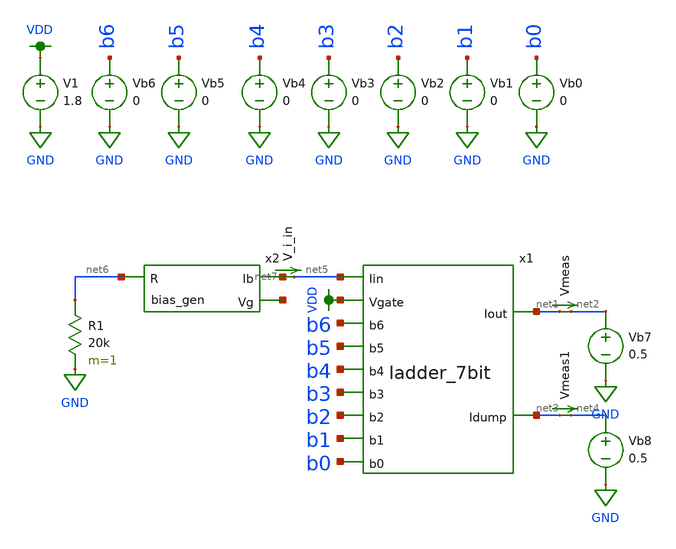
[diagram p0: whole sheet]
** sch_path: test_harness_mc.sch
**.subckt test_harness_mc
x1 VDD net5 net3 net1 b5 b4 b1 b2 b3 b0 b6 ladder_7bit
Vmeas net1 net2 0
.save i(vmeas)
Vb0 b0 GND 0
Vb1 b1 GND 0
Vb2 b2 GND 0
Vb3 b3 GND 0
Vb4 b4 GND 0
Vb5 b5 GND 0
Vb6 b6 GND 0
V1 VDD GND 1.8
Vb7 net2 GND 0.5
Vb8 net4 GND 0.5
Vmeas1 net3 net4 0
.save i(vmeas1)
V_i_in net7 net5 0
.save i(v_i_in)
x2 net7 net8 net6 bias_gen
R1 net6 GND 20k m=1
**** begin user architecture code

.option wnflag=1
.param MC_SWITCH=0.0
.lib ~/skywater/skywater-pdk/libraries/sky130_fd_pr_ngspice/latest/models/sky130.lib.spice tt


.control
  let runs = 10
  let run = 1
  while run <= runs
    set appendwrite = FALSE
    set wr_vecnames
    let code = 0
    while code < 128
      if code eq 0
        let b0 = 0
      else
        let b0 = code % 2
      end
      if floor(code / 2) eq 0
        let b1 = 0
      else
        let b1 = floor(code / 2) % 2
      end
      if floor(code / 4) eq 0
        let b2 = 0
      else
        let b2 = floor(code / 4) % 2
      end
      if floor(code / 8) eq 0
        let b3 = 0
      else
        let b3 = floor(code / 8) % 2
      end
      if floor(code / 16) eq 0
        let b4 = 0
      else
        let b4 = floor(code / 16) % 2
      end
      if floor(code / 32) eq 0
        let b5 = 0
      else
        let b5 = floor(code / 32) % 2
      end
      if floor(code / 64) eq 0
        let b6 = 0
      else
        let b6 = floor(code / 64) % 2
      end
      alter vb0 1.8*$&b0
      alter vb1 1.8*$&b1
      alter vb2 1.8*$&b2
      alter vb3 1.8*$&b3
      alter vb4 1.8*$&b4
      alter vb5 1.8*$&b5
      alter vb6 1.8*$&b6
      save all
      op
      wrdata ~/Documents/dac/mcdac{$&run}.txt v(b0) v(b1) v(b2) v(b3) v(b4) v(b5) v(b6) i(V_i_in) i(Vmeas)
+ i(Vmeas1)
      if code eq 0
        set appendwrite
        set wr_vecnames = FALSE
      end
      let code = code + 1
    end
    reset
    let run = run + 1
  end
.endc

**** end user architecture code
**.ends

* expanding   symbol:  ./ladder_7bit.sym # of pins=11
** sym_path: ladder_7bit.sym
** sch_path: ladder_7bit.sch
.subckt ladder_7bit Vgate Iin Idump Iout b5 b4 b1 b2 b3 b0 b6
*.opin Idump
*.opin Iout
*.ipin Vgate
*.ipin Iin
*.ipin b6
*.ipin b5
*.ipin b4
*.ipin b3
*.ipin b2
*.ipin b1
*.ipin b0
x1 Iin net8 Vgate Idump Iout net1 b6 ladder_1bit
x2 net8 net9 Vgate Idump Iout net2 b5 ladder_1bit
x3 net9 net10 Vgate Idump Iout net3 b4 ladder_1bit
x4 net10 net11 Vgate Idump Iout net4 b3 ladder_1bit
x5 net11 net12 Vgate Idump Iout net5 b2 ladder_1bit
x6 net12 net13 Vgate Idump Iout net6 b1 ladder_1bit
x7 net13 net14 Vgate Idump Iout net7 b0 ladder_1bit
XM1 Idump Vgate net14 GND sky130_fd_pr__nfet_01v8 L=0.15 W=1 nf=1 ad='int((nf+1)/2) * W/nf * 0.29' as='int((nf+2)/2) * W/nf * 0.29'
+ pd='2*int((nf+1)/2) * (W/nf + 0.29)' ps='2*int((nf+2)/2) * (W/nf + 0.29)' nrd='0.29 / W' nrs='0.29 / W'
+ sa=0 sb=0 sd=0 mult=1 m=1
X8 b6 net15 VDD GND inverter
X9 b5 net16 VDD GND inverter
X10 b4 net17 VDD GND inverter
X11 b3 net18 VDD GND inverter
X12 b2 net19 VDD GND inverter
X13 b1 net20 VDD GND inverter
X14 b0 net21 VDD GND inverter
.ends


* expanding   symbol:  ./bias_gen.sym # of pins=3
** sym_path: bias_gen.sym
** sch_path: bias_gen.sch
.subckt bias_gen Ib Vg R
*.ipin R
*.opin Ib
*.opin Vg
XM2 R net2 net2 GND sky130_fd_pr__nfet_01v8 L=4 W=96 nf=1 ad='int((nf+1)/2) * W/nf * 0.29' as='int((nf+2)/2) * W/nf * 0.29'
+ pd='2*int((nf+1)/2) * (W/nf + 0.29)' ps='2*int((nf+2)/2) * (W/nf + 0.29)' nrd='0.29 / W' nrs='0.29 / W'
+ sa=0 sb=0 sd=0 mult=1 m=1
XM3 VDD net1 net1 VDD sky130_fd_pr__pfet_01v8 L=4 W=12 nf=1 ad='int((nf+1)/2) * W/nf * 0.29' as='int((nf+2)/2) * W/nf * 0.29'
+ pd='2*int((nf+1)/2) * (W/nf + 0.29)' ps='2*int((nf+2)/2) * (W/nf + 0.29)' nrd='0.29 / W' nrs='0.29 / W'
+ sa=0 sb=0 sd=0 mult=1 m=1
XM1 VDD Vg net2 VDD sky130_fd_pr__pfet_01v8 L=4 W=12 nf=1 ad='int((nf+1)/2) * W/nf * 0.29' as='int((nf+2)/2) * W/nf * 0.29'
+ pd='2*int((nf+1)/2) * (W/nf + 0.29)' ps='2*int((nf+2)/2) * (W/nf + 0.29)' nrd='0.29 / W' nrs='0.29 / W'
+ sa=0 sb=0 sd=0 mult=1 m=1
XM4 Vg net1 VDD VDD sky130_fd_pr__pfet_01v8 L=4 W=12 nf=1 ad='int((nf+1)/2) * W/nf * 0.29' as='int((nf+2)/2) * W/nf * 0.29'
+ pd='2*int((nf+1)/2) * (W/nf + 0.29)' ps='2*int((nf+2)/2) * (W/nf + 0.29)' nrd='0.29 / W' nrs='0.29 / W'
+ sa=0 sb=0 sd=0 mult=1 m=1
XM5 net3 Vg VDD VDD sky130_fd_pr__pfet_01v8 L=4 W=12 nf=1 ad='int((nf+1)/2) * W/nf * 0.29' as='int((nf+2)/2) * W/nf * 0.29'
+ pd='2*int((nf+1)/2) * (W/nf + 0.29)' ps='2*int((nf+2)/2) * (W/nf + 0.29)' nrd='0.29 / W' nrs='0.29 / W'
+ sa=0 sb=0 sd=0 mult=1 m=1
XM7 Ib Vg VDD VDD sky130_fd_pr__pfet_01v8 L=4 W=12 nf=1 ad='int((nf+1)/2) * W/nf * 0.29' as='int((nf+2)/2) * W/nf * 0.29'
+ pd='2*int((nf+1)/2) * (W/nf + 0.29)' ps='2*int((nf+2)/2) * (W/nf + 0.29)' nrd='0.29 / W' nrs='0.29 / W'
+ sa=0 sb=0 sd=0 mult=1 m=1
XM6 net1 net2 GND GND sky130_fd_pr__nfet_01v8 L=4 W=12 nf=1 ad='int((nf+1)/2) * W/nf * 0.29' as='int((nf+2)/2) * W/nf * 0.29'
+ pd='2*int((nf+1)/2) * (W/nf + 0.29)' ps='2*int((nf+2)/2) * (W/nf + 0.29)' nrd='0.29 / W' nrs='0.29 / W'
+ sa=0 sb=0 sd=0 mult=1 m=1
XM8 GND net3 Vg GND sky130_fd_pr__nfet_01v8 L=4 W=12 nf=1 ad='int((nf+1)/2) * W/nf * 0.29' as='int((nf+2)/2) * W/nf * 0.29'
+ pd='2*int((nf+1)/2) * (W/nf + 0.29)' ps='2*int((nf+2)/2) * (W/nf + 0.29)' nrd='0.29 / W' nrs='0.29 / W'
+ sa=0 sb=0 sd=0 mult=1 m=1
XM9 net3 net3 GND GND sky130_fd_pr__nfet_01v8 L=4 W=12 nf=1 ad='int((nf+1)/2) * W/nf * 0.29' as='int((nf+2)/2) * W/nf * 0.29'
+ pd='2*int((nf+1)/2) * (W/nf + 0.29)' ps='2*int((nf+2)/2) * (W/nf + 0.29)' nrd='0.29 / W' nrs='0.29 / W'
+ sa=0 sb=0 sd=0 mult=1 m=1
.ends


* expanding   symbol:  /home/madvlsi/R2R-DAC/ladder_1bit.sym # of pins=7
** sym_path: ladder_1bit.sym
** sch_path: ladder_1bit.sch
.subckt ladder_1bit Iin_in Iin_out Vg I_dump Iout B_bar B
*.ipin Iin_in
*.ipin Vg
*.ipin B
*.ipin B_bar
*.opin Iin_out
*.opin I_dump
*.opin Iout
XM5 net1 Vg Iin_in GND sky130_fd_pr__nfet_01v8 L=0.15 W=1 nf=1 ad='int((nf+1)/2) * W/nf * 0.29' as='int((nf+2)/2) * W/nf * 0.29'
+ pd='2*int((nf+1)/2) * (W/nf + 0.29)' ps='2*int((nf+2)/2) * (W/nf + 0.29)' nrd='0.29 / W' nrs='0.29 / W'
+ sa=0 sb=0 sd=0 mult=1 m=1
XM6 Iout B net1 GND sky130_fd_pr__nfet_01v8 L=0.15 W=1 nf=1 ad='int((nf+1)/2) * W/nf * 0.29' as='int((nf+2)/2) * W/nf * 0.29'
+ pd='2*int((nf+1)/2) * (W/nf + 0.29)' ps='2*int((nf+2)/2) * (W/nf + 0.29)' nrd='0.29 / W' nrs='0.29 / W'
+ sa=0 sb=0 sd=0 mult=1 m=1
XM7 net1 B_bar I_dump GND sky130_fd_pr__nfet_01v8 L=0.15 W=1 nf=1 ad='int((nf+1)/2) * W/nf * 0.29' as='int((nf+2)/2) * W/nf * 0.29'
+ pd='2*int((nf+1)/2) * (W/nf + 0.29)' ps='2*int((nf+2)/2) * (W/nf + 0.29)' nrd='0.29 / W' nrs='0.29 / W'
+ sa=0 sb=0 sd=0 mult=1 m=1
XM8 Iin_in Vg Iin_out GND sky130_fd_pr__nfet_01v8 L=0.15 W=1 nf=1 ad='int((nf+1)/2) * W/nf * 0.29' as='int((nf+2)/2) * W/nf * 0.29'
+ pd='2*int((nf+1)/2) * (W/nf + 0.29)' ps='2*int((nf+2)/2) * (W/nf + 0.29)' nrd='0.29 / W' nrs='0.29 / W'
+ sa=0 sb=0 sd=0 mult=1 m=1
.ends


* expanding   symbol:  /home/madvlsi/Documents/mp1/inverter.sym # of pins=4
** sym_path: /home/madvlsi/Documents/mp1/inverter.sym
** sch_path: /home/madvlsi/Documents/mp1/inverter.sch
.subckt inverter A Y VP VN
*.ipin A
*.iopin VP
*.iopin VN
*.opin Y
XM3 Y A VP VP sky130_fd_pr__pfet_01v8 L=0.15 W=1 nf=1 ad='int((nf+1)/2) * W/nf * 0.29' as='int((nf+2)/2) * W/nf * 0.29'
+ pd='2*int((nf+1)/2) * (W/nf + 0.29)' ps='2*int((nf+2)/2) * (W/nf + 0.29)' nrd='0.29 / W' nrs='0.29 / W'
+ sa=0 sb=0 sd=0 mult=1 m=1
XM4 Y A VN VN sky130_fd_pr__nfet_01v8 L=0.15 W=1 nf=1 ad='int((nf+1)/2) * W/nf * 0.29' as='int((nf+2)/2) * W/nf * 0.29'
+ pd='2*int((nf+1)/2) * (W/nf + 0.29)' ps='2*int((nf+2)/2) * (W/nf + 0.29)' nrd='0.29 / W' nrs='0.29 / W'
+ sa=0 sb=0 sd=0 mult=1 m=1
.ends

.GLOBAL VDD
.GLOBAL GND
.end
